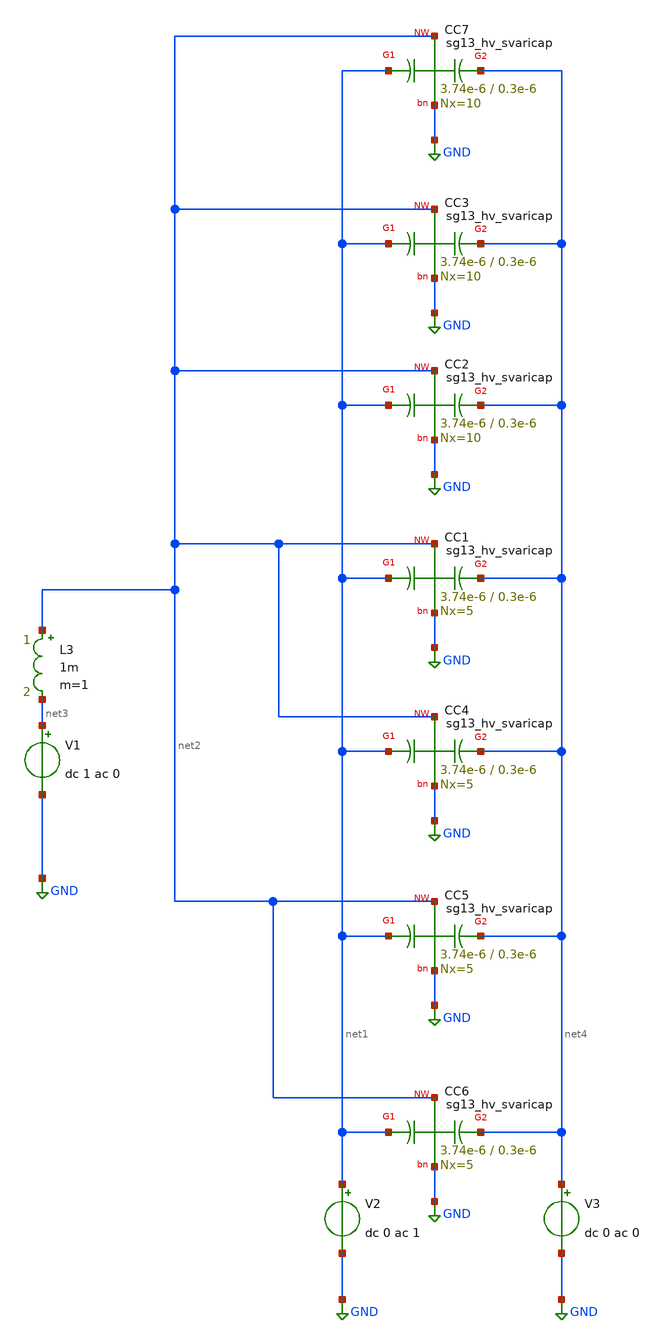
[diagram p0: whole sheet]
** sch_path: ihp-sg13g2/xschem_libs/sg13g2_tests_ase/ac_svaricap_test/schematic/ac_svaricap_test.sch
**.subckt ac_svaricap_test
XC1 net1 net2 net4 GND sg13_hv_svaricap w=3.74e-6 l=0.3e-6 Nx=5
V1 net3 GND dc 1 ac 0
L3 net2 net3 1m m=1
V3 net4 GND dc 0 ac 0
XC2 net1 net2 net4 GND sg13_hv_svaricap w=3.74e-6 l=0.3e-6 Nx=10
XC3 net1 net2 net4 GND sg13_hv_svaricap w=3.74e-6 l=0.3e-6 Nx=10
XC4 net1 net2 net4 GND sg13_hv_svaricap w=3.74e-6 l=0.3e-6 Nx=5
XC5 net1 net2 net4 GND sg13_hv_svaricap w=3.74e-6 l=0.3e-6 Nx=5
XC6 net1 net2 net4 GND sg13_hv_svaricap w=3.74e-6 l=0.3e-6 Nx=5
XC7 net1 net2 net4 GND sg13_hv_svaricap w=3.74e-6 l=0.3e-6 Nx=10
V2 net1 GND dc 0 ac 1
**.ends
.GLOBAL GND
.end
